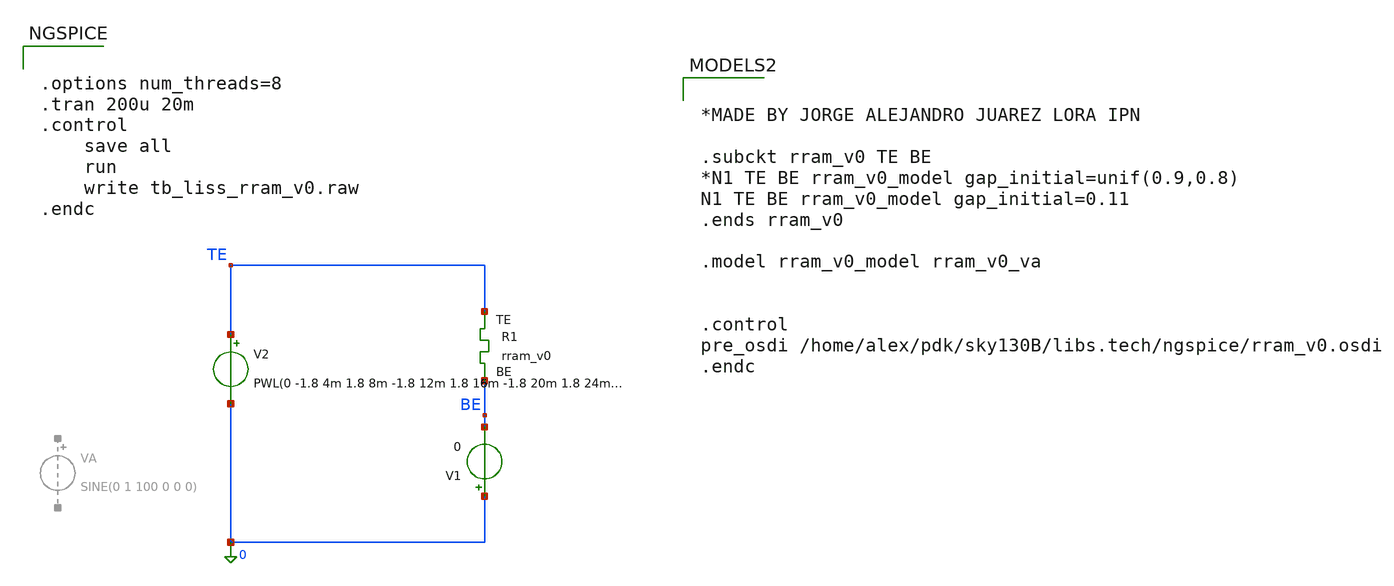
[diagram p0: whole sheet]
** sch_path: memristor_models/wellposed/tb_liss_rram_v0.sch
**.subckt tb_liss_rram_v0
XR1 TE BE rram_v0
V1 0 BE 0
V2 TE 0 PWL(0 -1.8 4m 1.8 8m -1.8 12m 1.8 16m -1.8 20m 1.8 24m -1.8)
**** begin user architecture code


.options num_threads=8
.tran 200u 20m
.control
	save all
	run
	write tb_liss_rram_v0.raw
.endc




*MADE BY JORGE ALEJANDRO JUAREZ LORA IPN

.subckt rram_v0 TE BE
*N1 TE BE rram_v0_model gap_initial=unif(0.9,0.8)
N1 TE BE rram_v0_model gap_initial=0.11
.ends rram_v0

.model rram_v0_model rram_v0_va


.control
pre_osdi /home/alex/pdk/sky130B/libs.tech/ngspice/rram_v0.osdi
.endc

**** end user architecture code
**.ends
.end
